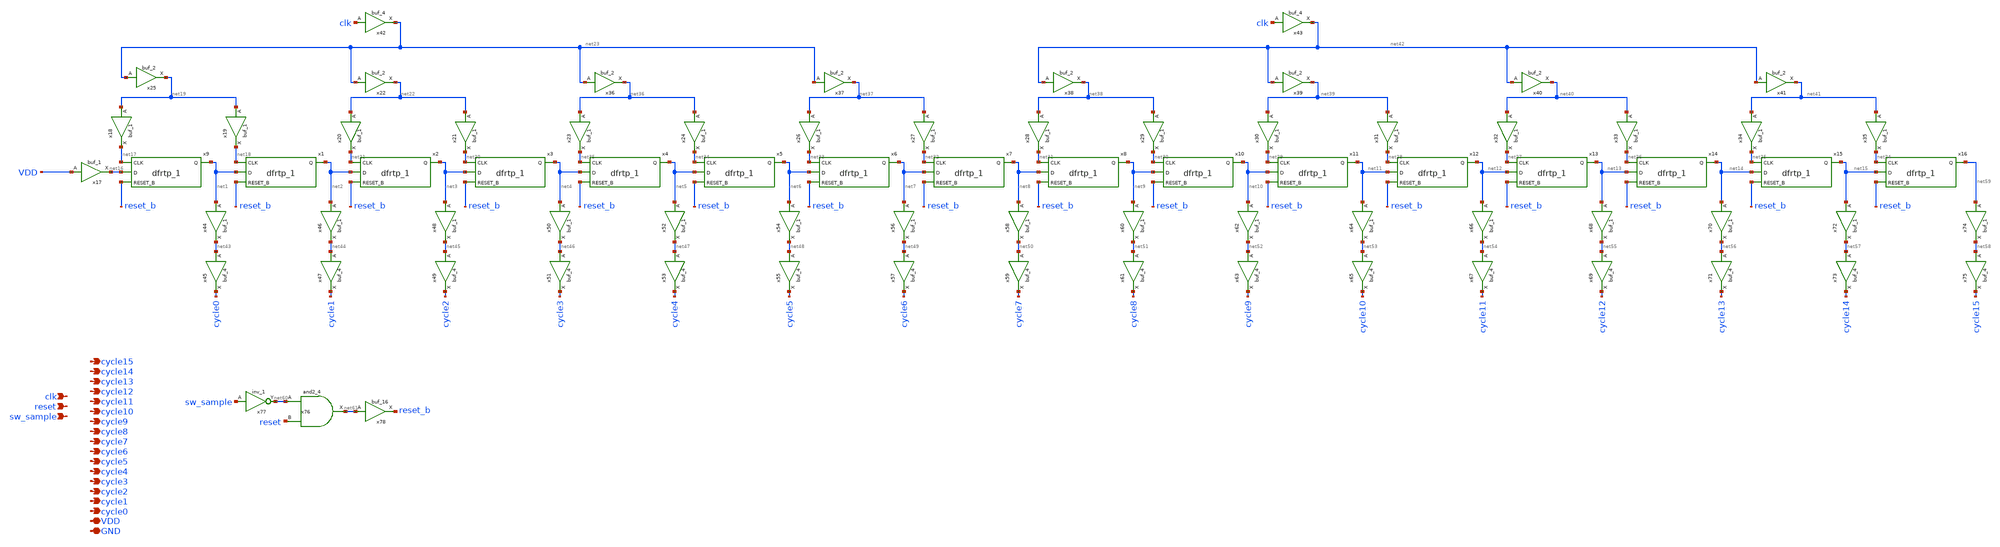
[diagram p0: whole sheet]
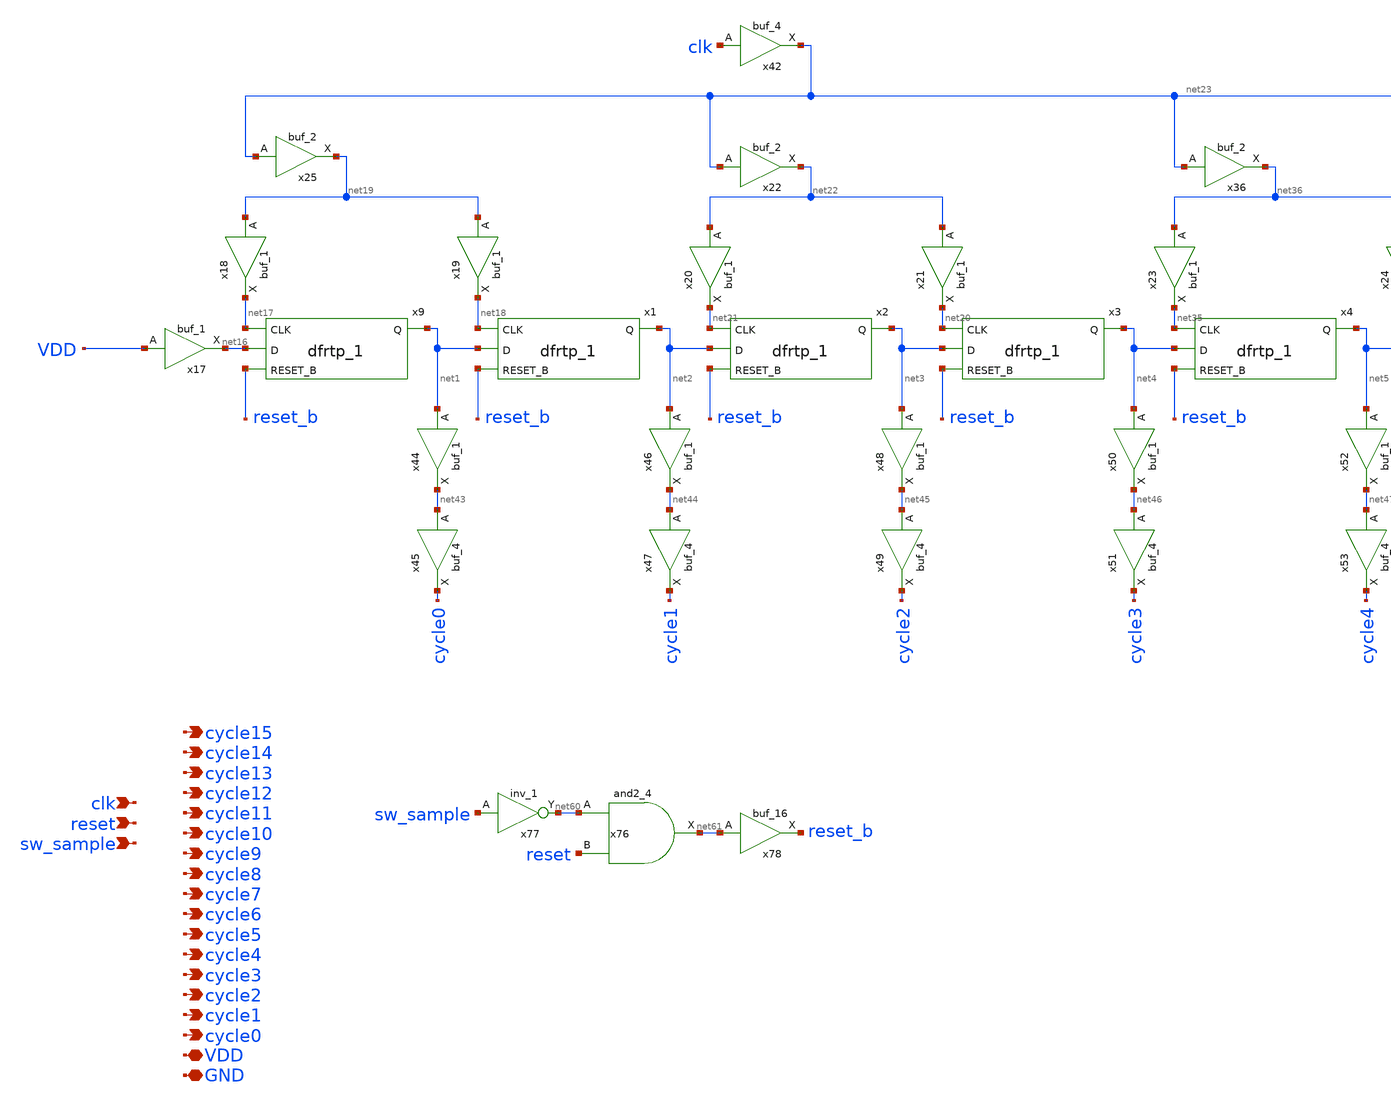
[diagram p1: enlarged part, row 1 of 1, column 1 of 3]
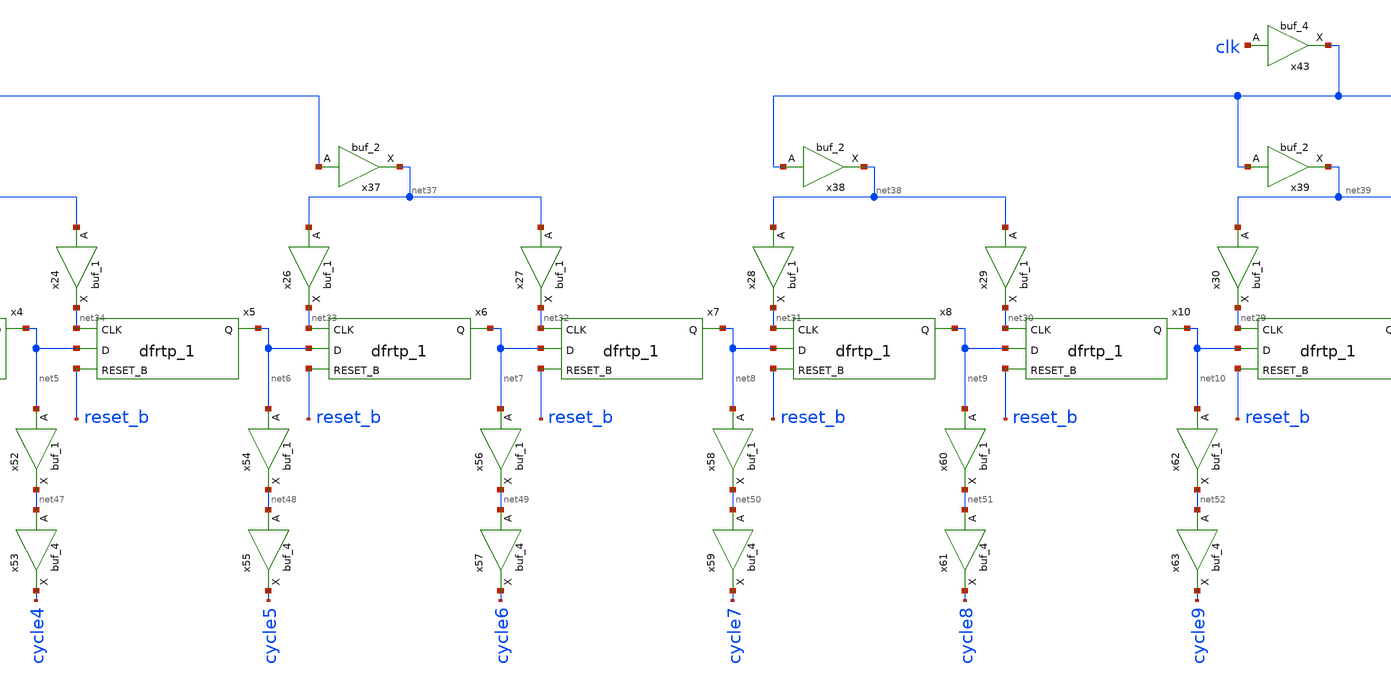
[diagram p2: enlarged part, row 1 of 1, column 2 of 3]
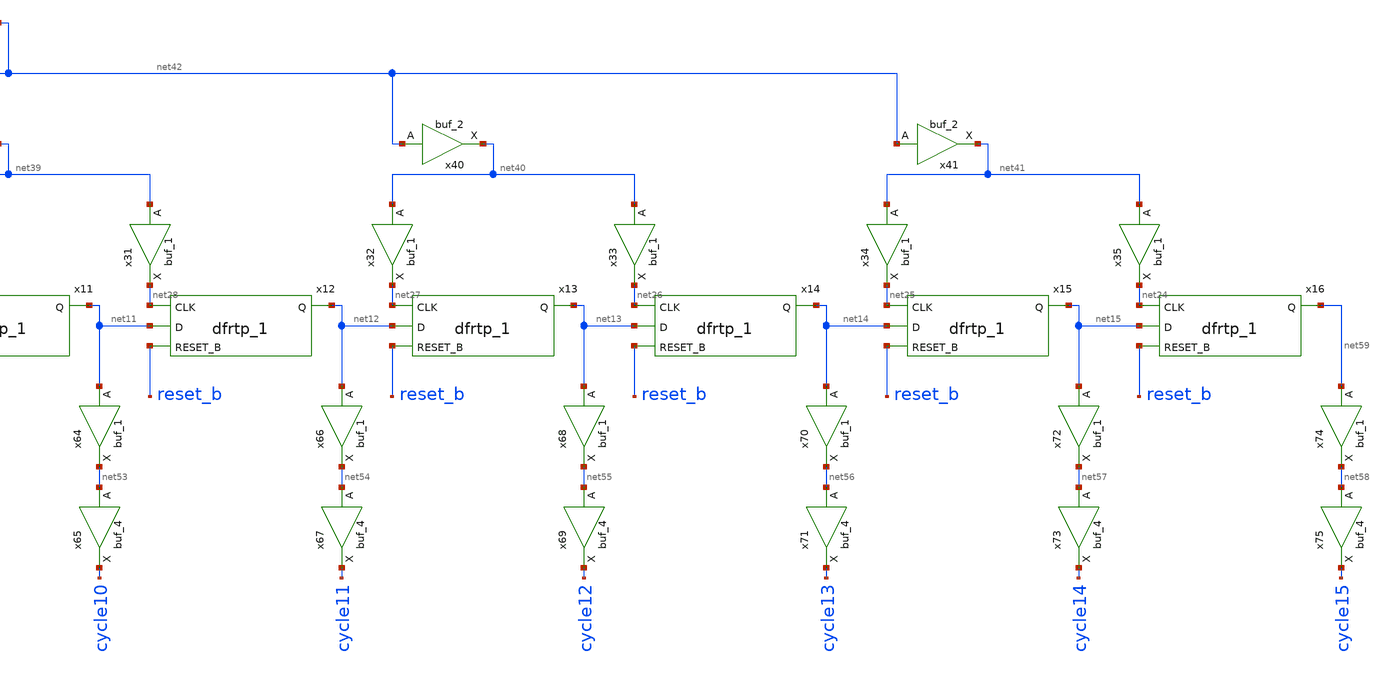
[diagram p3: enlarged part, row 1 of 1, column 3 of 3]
** sch_path: xschem/shiftedclockgen/shifted_clkgen.sch
**.subckt shifted_clkgen clk sw_sample VDD GND reset cycle15 cycle14 cycle13 cycle12 cycle11 cycle10
*+ cycle9 cycle8 cycle7 cycle6 cycle5 cycle4 cycle3 cycle2 cycle1 cycle0
*.ipin clk
*.ipin sw_sample
*.iopin VDD
*.iopin GND
*.ipin reset
*.opin cycle15
*.opin cycle14
*.opin cycle13
*.opin cycle12
*.opin cycle11
*.opin cycle10
*.opin cycle9
*.opin cycle8
*.opin cycle7
*.opin cycle6
*.opin cycle5
*.opin cycle4
*.opin cycle3
*.opin cycle2
*.opin cycle1
*.opin cycle0
x9 net17 net16 reset_b GND GND VDD VDD net1 sky130_fd_sc_hd__dfrtp_1
x1 net18 net1 reset_b GND GND VDD VDD net2 sky130_fd_sc_hd__dfrtp_1
x2 net21 net2 reset_b GND GND VDD VDD net3 sky130_fd_sc_hd__dfrtp_1
x3 net20 net3 reset_b GND GND VDD VDD net4 sky130_fd_sc_hd__dfrtp_1
x4 net35 net4 reset_b GND GND VDD VDD net5 sky130_fd_sc_hd__dfrtp_1
x5 net34 net5 reset_b GND GND VDD VDD net6 sky130_fd_sc_hd__dfrtp_1
x6 net33 net6 reset_b GND GND VDD VDD net7 sky130_fd_sc_hd__dfrtp_1
x7 net32 net7 reset_b GND GND VDD VDD net8 sky130_fd_sc_hd__dfrtp_1
x8 net31 net8 reset_b GND GND VDD VDD net9 sky130_fd_sc_hd__dfrtp_1
x10 net30 net9 reset_b GND GND VDD VDD net10 sky130_fd_sc_hd__dfrtp_1
x11 net29 net10 reset_b GND GND VDD VDD net11 sky130_fd_sc_hd__dfrtp_1
x12 net28 net11 reset_b GND GND VDD VDD net12 sky130_fd_sc_hd__dfrtp_1
x13 net27 net12 reset_b GND GND VDD VDD net13 sky130_fd_sc_hd__dfrtp_1
x14 net26 net13 reset_b GND GND VDD VDD net14 sky130_fd_sc_hd__dfrtp_1
x15 net25 net14 reset_b GND GND VDD VDD net15 sky130_fd_sc_hd__dfrtp_1
x16 net24 net15 reset_b GND GND VDD VDD net59 sky130_fd_sc_hd__dfrtp_1
x17 VDD GND GND VDD VDD net16 sky130_fd_sc_hd__buf_1
x18 net19 GND GND VDD VDD net17 sky130_fd_sc_hd__buf_1
x19 net19 GND GND VDD VDD net18 sky130_fd_sc_hd__buf_1
x25 net23 GND GND VDD VDD net19 sky130_fd_sc_hd__buf_2
x20 net22 GND GND VDD VDD net21 sky130_fd_sc_hd__buf_1
x21 net22 GND GND VDD VDD net20 sky130_fd_sc_hd__buf_1
x22 net23 GND GND VDD VDD net22 sky130_fd_sc_hd__buf_2
x23 net36 GND GND VDD VDD net35 sky130_fd_sc_hd__buf_1
x24 net36 GND GND VDD VDD net34 sky130_fd_sc_hd__buf_1
x26 net37 GND GND VDD VDD net33 sky130_fd_sc_hd__buf_1
x27 net37 GND GND VDD VDD net32 sky130_fd_sc_hd__buf_1
x28 net38 GND GND VDD VDD net31 sky130_fd_sc_hd__buf_1
x29 net38 GND GND VDD VDD net30 sky130_fd_sc_hd__buf_1
x30 net39 GND GND VDD VDD net29 sky130_fd_sc_hd__buf_1
x31 net39 GND GND VDD VDD net28 sky130_fd_sc_hd__buf_1
x32 net40 GND GND VDD VDD net27 sky130_fd_sc_hd__buf_1
x33 net40 GND GND VDD VDD net26 sky130_fd_sc_hd__buf_1
x34 net41 GND GND VDD VDD net25 sky130_fd_sc_hd__buf_1
x35 net41 GND GND VDD VDD net24 sky130_fd_sc_hd__buf_1
x36 net23 GND GND VDD VDD net36 sky130_fd_sc_hd__buf_2
x37 net23 GND GND VDD VDD net37 sky130_fd_sc_hd__buf_2
x38 net42 GND GND VDD VDD net38 sky130_fd_sc_hd__buf_2
x39 net42 GND GND VDD VDD net39 sky130_fd_sc_hd__buf_2
x40 net42 GND GND VDD VDD net40 sky130_fd_sc_hd__buf_2
x41 net42 GND GND VDD VDD net41 sky130_fd_sc_hd__buf_2
x42 clk GND GND VDD VDD net23 sky130_fd_sc_hd__buf_4
x43 clk GND GND VDD VDD net42 sky130_fd_sc_hd__buf_4
x44 net1 GND GND VDD VDD net43 sky130_fd_sc_hd__buf_1
x45 net43 GND GND VDD VDD cycle0 sky130_fd_sc_hd__buf_4
x46 net2 GND GND VDD VDD net44 sky130_fd_sc_hd__buf_1
x47 net44 GND GND VDD VDD cycle1 sky130_fd_sc_hd__buf_4
x48 net3 GND GND VDD VDD net45 sky130_fd_sc_hd__buf_1
x49 net45 GND GND VDD VDD cycle2 sky130_fd_sc_hd__buf_4
x50 net4 GND GND VDD VDD net46 sky130_fd_sc_hd__buf_1
x51 net46 GND GND VDD VDD cycle3 sky130_fd_sc_hd__buf_4
x52 net5 GND GND VDD VDD net47 sky130_fd_sc_hd__buf_1
x53 net47 GND GND VDD VDD cycle4 sky130_fd_sc_hd__buf_4
x54 net6 GND GND VDD VDD net48 sky130_fd_sc_hd__buf_1
x55 net48 GND GND VDD VDD cycle5 sky130_fd_sc_hd__buf_4
x56 net7 GND GND VDD VDD net49 sky130_fd_sc_hd__buf_1
x57 net49 GND GND VDD VDD cycle6 sky130_fd_sc_hd__buf_4
x58 net8 GND GND VDD VDD net50 sky130_fd_sc_hd__buf_1
x59 net50 GND GND VDD VDD cycle7 sky130_fd_sc_hd__buf_4
x60 net9 GND GND VDD VDD net51 sky130_fd_sc_hd__buf_1
x61 net51 GND GND VDD VDD cycle8 sky130_fd_sc_hd__buf_4
x62 net10 GND GND VDD VDD net52 sky130_fd_sc_hd__buf_1
x63 net52 GND GND VDD VDD cycle9 sky130_fd_sc_hd__buf_4
x64 net11 GND GND VDD VDD net53 sky130_fd_sc_hd__buf_1
x65 net53 GND GND VDD VDD cycle10 sky130_fd_sc_hd__buf_4
x66 net12 GND GND VDD VDD net54 sky130_fd_sc_hd__buf_1
x67 net54 GND GND VDD VDD cycle11 sky130_fd_sc_hd__buf_4
x68 net13 GND GND VDD VDD net55 sky130_fd_sc_hd__buf_1
x69 net55 GND GND VDD VDD cycle12 sky130_fd_sc_hd__buf_4
x70 net14 GND GND VDD VDD net56 sky130_fd_sc_hd__buf_1
x71 net56 GND GND VDD VDD cycle13 sky130_fd_sc_hd__buf_4
x72 net15 GND GND VDD VDD net57 sky130_fd_sc_hd__buf_1
x73 net57 GND GND VDD VDD cycle14 sky130_fd_sc_hd__buf_4
x74 net59 GND GND VDD VDD net58 sky130_fd_sc_hd__buf_1
x75 net58 GND GND VDD VDD cycle15 sky130_fd_sc_hd__buf_4
x76 net60 reset GND GND VDD VDD net61 sky130_fd_sc_hd__and2_4
x77 sw_sample GND GND VDD VDD net60 sky130_fd_sc_hd__inv_1
x78 net61 GND GND VDD VDD reset_b sky130_fd_sc_hd__buf_16
**.ends
.end
